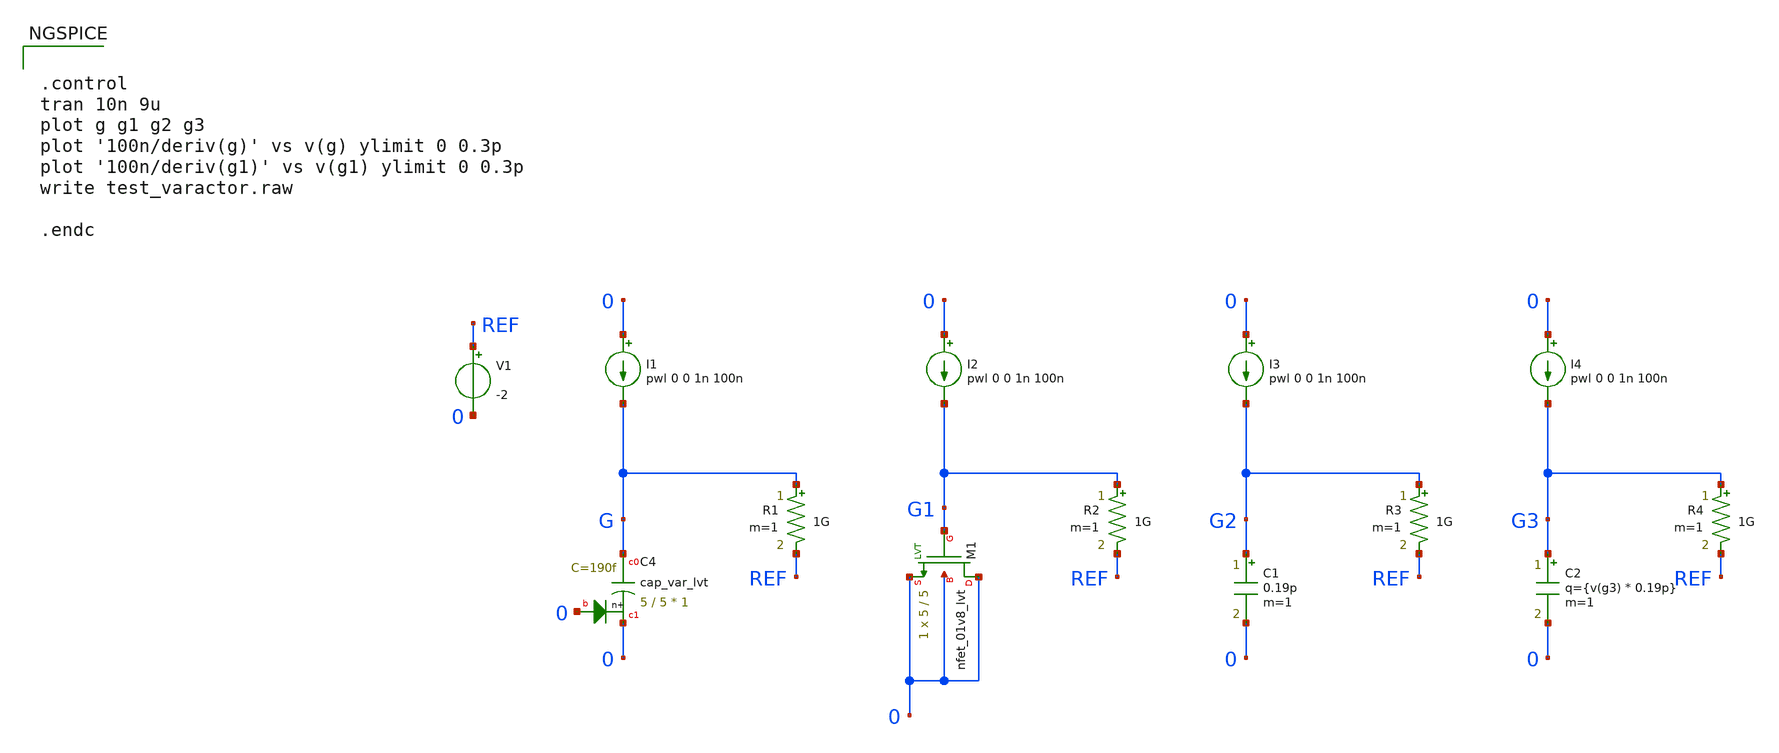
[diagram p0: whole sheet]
** sch_path: sky130_tests/test_varactor.sch
* Copyright 2021 Stefan Frederik Schippers
* Licensed under the Apache License, Version 2.0 (the "License");
* you may not use this file except in compliance with the License.
* You may obtain a copy of the License at
* https://www.apache.org/licenses/LICENSE-2.0
* Unless required by applicable law or agreed to in writing, software
* distributed under the License is distributed on an "AS IS" BASIS,
* WITHOUT WARRANTIES OR CONDITIONS OF ANY KIND, either express or implied.
* See the License for the specific language governing permissions and
* limitations under the License.
**.subckt test_varactor
I1 0 G pwl 0 0 1n 100n
R1 G REF 1G m=1
I2 0 G1 pwl 0 0 1n 100n
R2 G1 REF 1G m=1
I3 0 G2 pwl 0 0 1n 100n
R3 G2 REF 1G m=1
C1 G2 0 0.19p m=1
V1 REF 0 -2
XM1 0 G1 0 0 sky130_fd_pr__nfet_01v8_lvt L=5 W=5 nf=1 ad='W * 0.29' as='W * 0.29' pd='2 * (W + 0.29)'
+ ps='2 * (W + 0.29)' nrd='0.29 / W' nrs='0.29 / W' sa=0 sb=0 sd=0 mult=1 m=1
I4 0 G3 pwl 0 0 1n 100n
R4 G3 REF 1G m=1
C2 G3 0 q={v(g3) * 0.19p} m=1
XC4 G 0 0 sky130_fd_pr__cap_var_lvt W=5 L=5 VM=1 m=1
**** begin user architecture code


.control
tran 10n 9u
plot g g1 g2 g3
plot '100n/deriv(g)' vs v(g) ylimit 0 0.3p
plot '100n/deriv(g1)' vs v(g1) ylimit 0 0.3p
write test_varactor.raw

.endc


 ** manual skywater pdks install (with patches applied)
* .lib $::SKYWATER_MODELS/models/sky130.lib.spice tt

** opencircuitdesign pdks install
.lib $::SKYWATER_MODELS/sky130.lib.spice tt

.param mc_mm_switch=0
.param mc_pr_switch=0

**** end user architecture code
**.ends
.end
